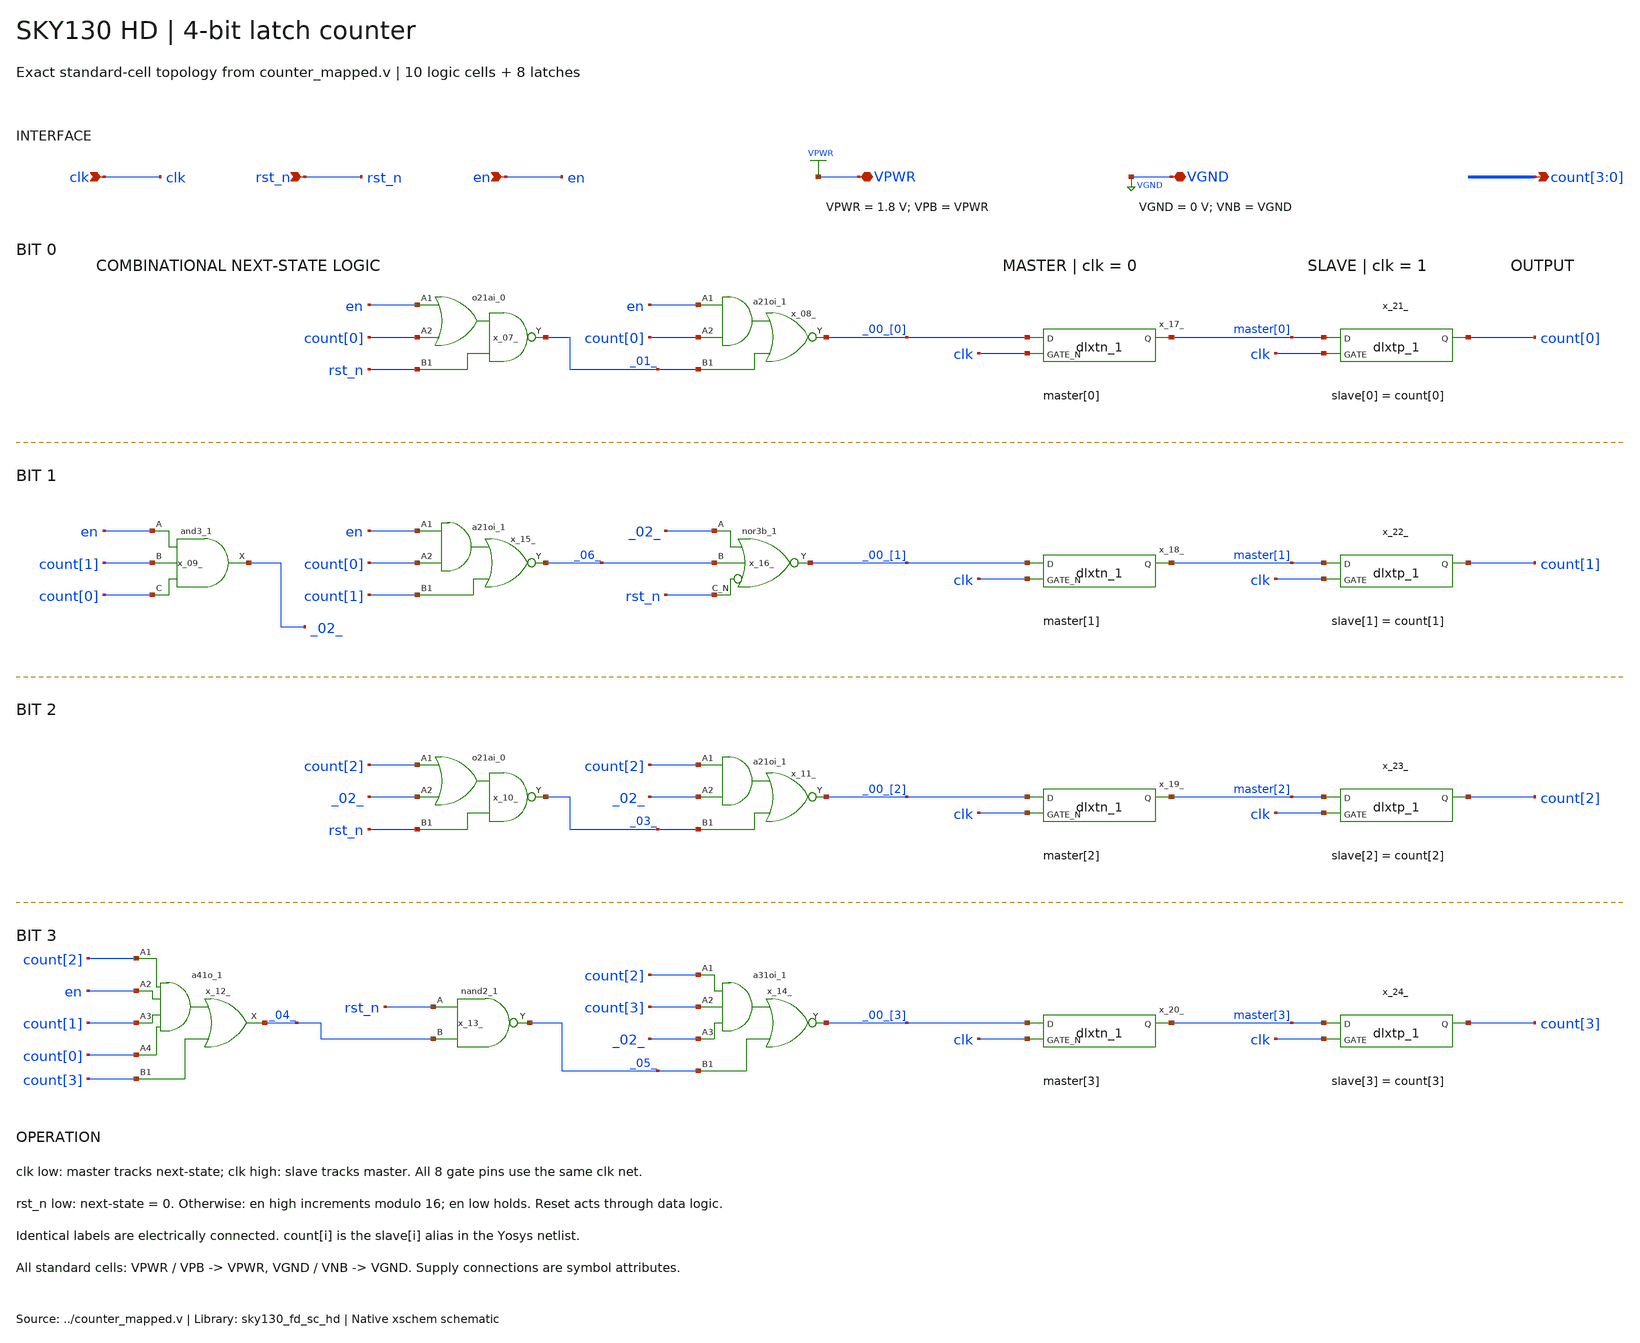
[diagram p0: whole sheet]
** sch_path: examples/counter/xschem/counter.sch
**.subckt counter clk rst_n en VPWR VGND count[3],count[2],count[1],count[0]
*.ipin clk
*.ipin rst_n
*.ipin en
*.iopin VPWR
*.iopin VGND
*.opin count[3],count[2],count[1],count[0]
x_07_ en count[0] rst_n VGND VGND VPWR VPWR _01_ sky130_fd_sc_hd__o21ai_0
x_08_ en count[0] _01_ VGND VGND VPWR VPWR _00_[0] sky130_fd_sc_hd__a21oi_1
x_09_ en count[1] count[0] VGND VGND VPWR VPWR _02_ sky130_fd_sc_hd__and3_1
x_10_ count[2] _02_ rst_n VGND VGND VPWR VPWR _03_ sky130_fd_sc_hd__o21ai_0
x_11_ count[2] _02_ _03_ VGND VGND VPWR VPWR _00_[2] sky130_fd_sc_hd__a21oi_1
x_12_ count[2] en count[1] count[0] count[3] VGND VGND VPWR VPWR _04_ sky130_fd_sc_hd__a41o_1
x_13_ rst_n _04_ VGND VGND VPWR VPWR _05_ sky130_fd_sc_hd__nand2_1
x_14_ count[2] count[3] _02_ _05_ VGND VGND VPWR VPWR _00_[3] sky130_fd_sc_hd__a31oi_1
x_15_ en count[0] count[1] VGND VGND VPWR VPWR _06_ sky130_fd_sc_hd__a21oi_1
x_16_ _02_ _06_ rst_n VGND VGND VPWR VPWR _00_[1] sky130_fd_sc_hd__nor3b_1
x_17_ _00_[0] clk VGND VGND VPWR VPWR master[0] sky130_fd_sc_hd__dlxtn_1
x_18_ _00_[1] clk VGND VGND VPWR VPWR master[1] sky130_fd_sc_hd__dlxtn_1
x_19_ _00_[2] clk VGND VGND VPWR VPWR master[2] sky130_fd_sc_hd__dlxtn_1
x_20_ _00_[3] clk VGND VGND VPWR VPWR master[3] sky130_fd_sc_hd__dlxtn_1
x_21_ master[0] clk VGND VGND VPWR VPWR count[0] sky130_fd_sc_hd__dlxtp_1
x_22_ master[1] clk VGND VGND VPWR VPWR count[1] sky130_fd_sc_hd__dlxtp_1
x_23_ master[2] clk VGND VGND VPWR VPWR count[2] sky130_fd_sc_hd__dlxtp_1
x_24_ master[3] clk VGND VGND VPWR VPWR count[3] sky130_fd_sc_hd__dlxtp_1
**.ends
.GLOBAL VPWR
.GLOBAL VGND
.end
